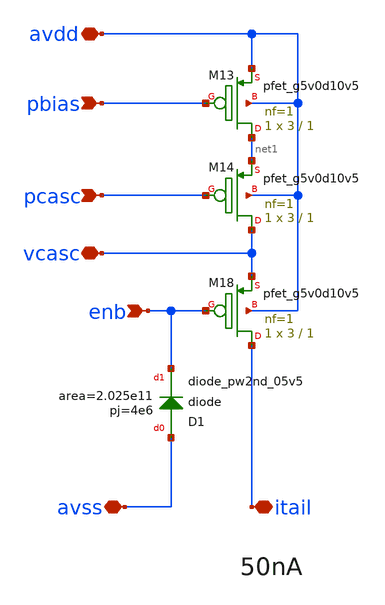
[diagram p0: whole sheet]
** sch_path: xschem/bias_pstack.sch
**.subckt bias_pstack avdd itail enb pcasc vcasc pbias avss
*.iopin avdd
*.iopin itail
*.ipin enb
*.ipin pcasc
*.iopin vcasc
*.ipin pbias
*.iopin avss
XM13 net1 pbias avdd avdd sky130_fd_pr__pfet_g5v0d10v5 L=1 W=3 nf=1 ad='int((nf+1)/2) * W/nf * 0.29'
+ as='int((nf+2)/2) * W/nf * 0.29' pd='2*int((nf+1)/2) * (W/nf + 0.29)' ps='2*int((nf+2)/2) * (W/nf + 0.29)'
+ nrd='0.29 / W' nrs='0.29 / W' sa=0 sb=0 sd=0 mult=1 m=1
XM18 itail enb vcasc avdd sky130_fd_pr__pfet_g5v0d10v5 L=1 W=3 nf=1 ad='int((nf+1)/2) * W/nf * 0.29'
+ as='int((nf+2)/2) * W/nf * 0.29' pd='2*int((nf+1)/2) * (W/nf + 0.29)' ps='2*int((nf+2)/2) * (W/nf + 0.29)'
+ nrd='0.29 / W' nrs='0.29 / W' sa=0 sb=0 sd=0 mult=1 m=1
XM14 vcasc pcasc net1 avdd sky130_fd_pr__pfet_g5v0d10v5 L=1 W=3 nf=1 ad='int((nf+1)/2) * W/nf * 0.29'
+ as='int((nf+2)/2) * W/nf * 0.29' pd='2*int((nf+1)/2) * (W/nf + 0.29)' ps='2*int((nf+2)/2) * (W/nf + 0.29)'
+ nrd='0.29 / W' nrs='0.29 / W' sa=0 sb=0 sd=0 mult=1 m=1
XD1 avss enb sky130_fd_pr__diode_pw2nd_05v5 area=2.025e11 pj=4e6
**.ends
.end
